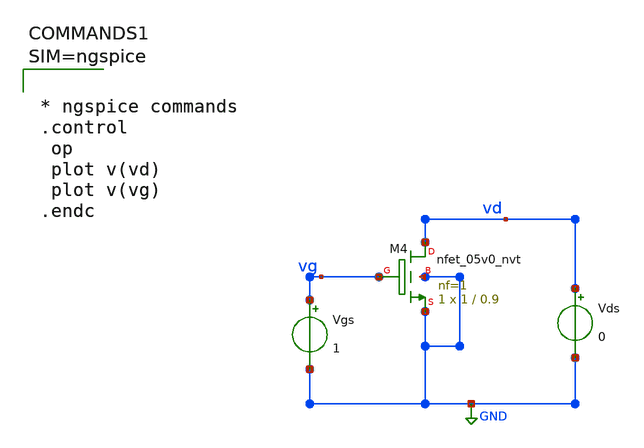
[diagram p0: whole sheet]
** sch_path: xschem/nfet_M4.sch
**.subckt nfet_M4
Vgs vg GND 1
Vds vd GND 0
XM4 vd vg GND GND sky130_fd_pr__nfet_05v0_nvt L=0.9 W=1 nf=1 ad='int((1 + 1)/2) * 1 / 1 * 0.29' as='int((1 + 2)/2) * 1 / 1 * 0.29'
+ pd='2*int((1 + 1)/2) * (1 / 1 + 0.29)' ps='2*int((1 + 2)/2) * (1 / 1 + 0.29)' nrd='0.29 / 1 ' nrs='0.29 / 1 '
+ sa=0 sb=0 sd=0 mult=1 m=1
**** begin user architecture code

** opencircuitdesign pdks install
.lib $::SKYWATER_MODELS/sky130.lib.spice tt




* ngspice commands
.control
 op
 plot v(vd)
 plot v(vg)
.endc




** opencircuitdesign pdks install
.lib $::SKYWATER_MODELS/sky130.lib.spice tt




* ngspice commands
.control
 op
 plot v(vd)
 plot v(vg)
.endc



**** end user architecture code
**.ends
.GLOBAL GND
.end
